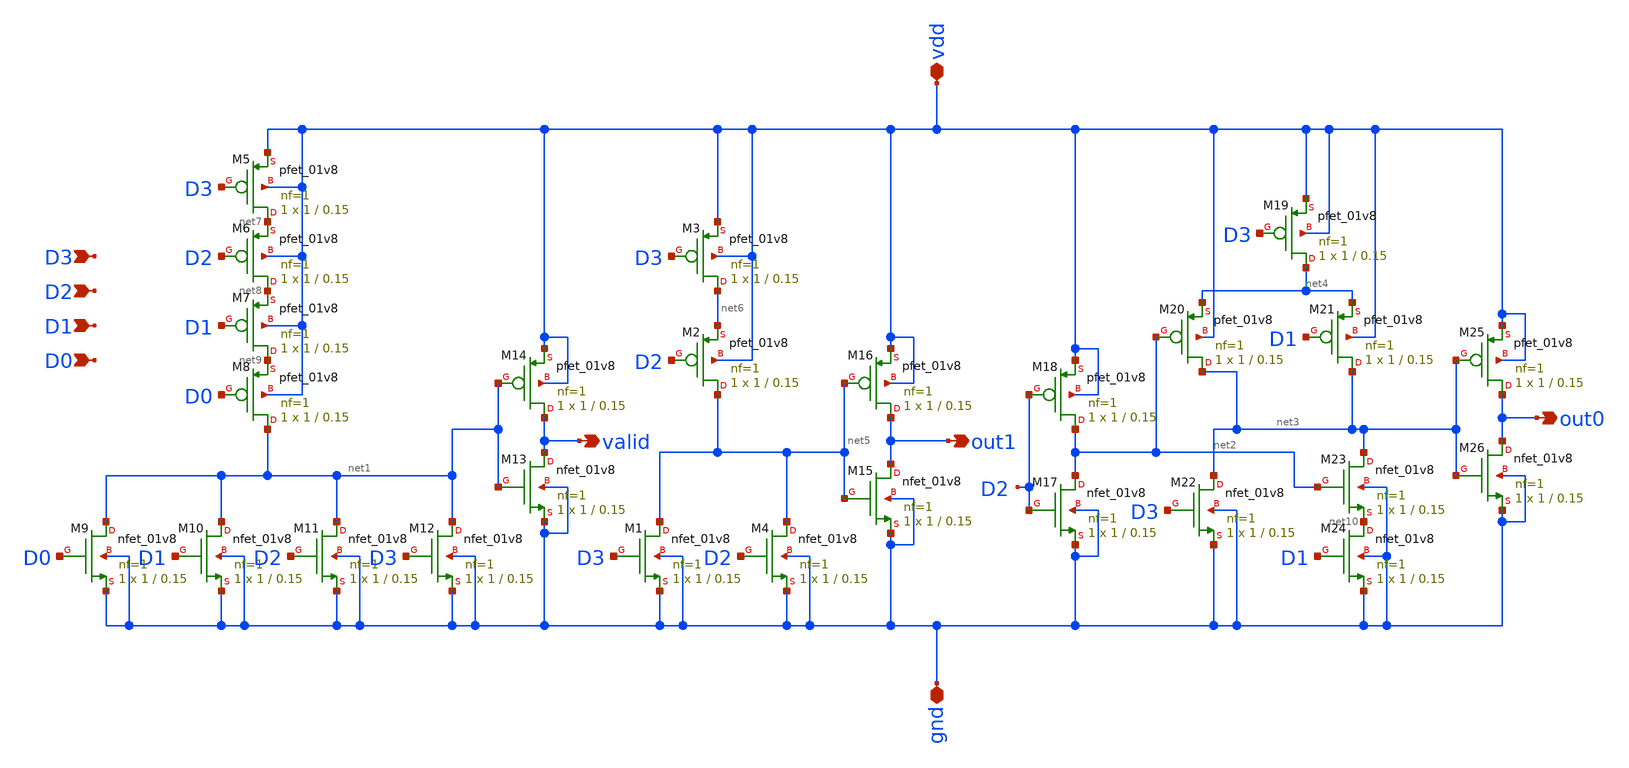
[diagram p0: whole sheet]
** sch_path: Primitives/Priority Encoder 4to2/Xschem Files/P_enc_4to2.sch
**.subckt P_enc_4to2 valid vdd gnd out1 out0 D3 D2 D1 D0
*.opin valid
*.iopin vdd
*.iopin gnd
*.opin out1
*.opin out0
*.ipin D3
*.ipin D2
*.ipin D1
*.ipin D0
XM5 net7 D3 vdd vdd sky130_fd_pr__pfet_01v8 L=0.15 W=1 nf=1 ad='int((1 + 1)/2) * 1 / 1 * 0.29' as='int((1 + 2)/2) * 1 / 1 * 0.29'
+ pd='2*int((1 + 1)/2) * (1 / 1 + 0.29)' ps='2*int((1 + 2)/2) * (1 / 1 + 0.29)' nrd='0.29 / 1 ' nrs='0.29 / 1 '
+ sa=0 sb=0 sd=0 mult=1 m=1
XM6 net8 D2 net7 vdd sky130_fd_pr__pfet_01v8 L=0.15 W=1 nf=1 ad='int((1 + 1)/2) * 1 / 1 * 0.29' as='int((1 + 2)/2) * 1 / 1 * 0.29'
+ pd='2*int((1 + 1)/2) * (1 / 1 + 0.29)' ps='2*int((1 + 2)/2) * (1 / 1 + 0.29)' nrd='0.29 / 1 ' nrs='0.29 / 1 '
+ sa=0 sb=0 sd=0 mult=1 m=1
XM7 net9 D1 net8 vdd sky130_fd_pr__pfet_01v8 L=0.15 W=1 nf=1 ad='int((1 + 1)/2) * 1 / 1 * 0.29' as='int((1 + 2)/2) * 1 / 1 * 0.29'
+ pd='2*int((1 + 1)/2) * (1 / 1 + 0.29)' ps='2*int((1 + 2)/2) * (1 / 1 + 0.29)' nrd='0.29 / 1 ' nrs='0.29 / 1 '
+ sa=0 sb=0 sd=0 mult=1 m=1
XM8 net1 D0 net9 vdd sky130_fd_pr__pfet_01v8 L=0.15 W=1 nf=1 ad='int((1 + 1)/2) * 1 / 1 * 0.29' as='int((1 + 2)/2) * 1 / 1 * 0.29'
+ pd='2*int((1 + 1)/2) * (1 / 1 + 0.29)' ps='2*int((1 + 2)/2) * (1 / 1 + 0.29)' nrd='0.29 / 1 ' nrs='0.29 / 1 '
+ sa=0 sb=0 sd=0 mult=1 m=1
XM9 net1 D0 gnd gnd sky130_fd_pr__nfet_01v8 L=0.15 W=1 nf=1 ad='int((1 + 1)/2) * 1 / 1 * 0.29' as='int((1 + 2)/2) * 1 / 1 * 0.29'
+ pd='2*int((1 + 1)/2) * (1 / 1 + 0.29)' ps='2*int((1 + 2)/2) * (1 / 1 + 0.29)' nrd='0.29 / 1 ' nrs='0.29 / 1 '
+ sa=0 sb=0 sd=0 mult=1 m=1
XM10 net1 D1 gnd gnd sky130_fd_pr__nfet_01v8 L=0.15 W=1 nf=1 ad='int((1 + 1)/2) * 1 / 1 * 0.29' as='int((1 + 2)/2) * 1 / 1 * 0.29'
+ pd='2*int((1 + 1)/2) * (1 / 1 + 0.29)' ps='2*int((1 + 2)/2) * (1 / 1 + 0.29)' nrd='0.29 / 1 ' nrs='0.29 / 1 '
+ sa=0 sb=0 sd=0 mult=1 m=1
XM11 net1 D2 gnd gnd sky130_fd_pr__nfet_01v8 L=0.15 W=1 nf=1 ad='int((1 + 1)/2) * 1 / 1 * 0.29' as='int((1 + 2)/2) * 1 / 1 * 0.29'
+ pd='2*int((1 + 1)/2) * (1 / 1 + 0.29)' ps='2*int((1 + 2)/2) * (1 / 1 + 0.29)' nrd='0.29 / 1 ' nrs='0.29 / 1 '
+ sa=0 sb=0 sd=0 mult=1 m=1
XM12 net1 D3 gnd gnd sky130_fd_pr__nfet_01v8 L=0.15 W=1 nf=1 ad='int((1 + 1)/2) * 1 / 1 * 0.29' as='int((1 + 2)/2) * 1 / 1 * 0.29'
+ pd='2*int((1 + 1)/2) * (1 / 1 + 0.29)' ps='2*int((1 + 2)/2) * (1 / 1 + 0.29)' nrd='0.29 / 1 ' nrs='0.29 / 1 '
+ sa=0 sb=0 sd=0 mult=1 m=1
XM13 valid net1 gnd gnd sky130_fd_pr__nfet_01v8 L=0.15 W=1 nf=1 ad='int((1 + 1)/2) * 1 / 1 * 0.29' as='int((1 + 2)/2) * 1 / 1 * 0.29'
+ pd='2*int((1 + 1)/2) * (1 / 1 + 0.29)' ps='2*int((1 + 2)/2) * (1 / 1 + 0.29)' nrd='0.29 / 1 ' nrs='0.29 / 1 '
+ sa=0 sb=0 sd=0 mult=1 m=1
XM14 valid net1 vdd vdd sky130_fd_pr__pfet_01v8 L=0.15 W=1 nf=1 ad='int((1 + 1)/2) * 1 / 1 * 0.29' as='int((1 + 2)/2) * 1 / 1 * 0.29'
+ pd='2*int((1 + 1)/2) * (1 / 1 + 0.29)' ps='2*int((1 + 2)/2) * (1 / 1 + 0.29)' nrd='0.29 / 1 ' nrs='0.29 / 1 '
+ sa=0 sb=0 sd=0 mult=1 m=1
XM17 net2 D2 gnd gnd sky130_fd_pr__nfet_01v8 L=0.15 W=1 nf=1 ad='int((1 + 1)/2) * 1 / 1 * 0.29' as='int((1 + 2)/2) * 1 / 1 * 0.29'
+ pd='2*int((1 + 1)/2) * (1 / 1 + 0.29)' ps='2*int((1 + 2)/2) * (1 / 1 + 0.29)' nrd='0.29 / 1 ' nrs='0.29 / 1 '
+ sa=0 sb=0 sd=0 mult=1 m=1
XM18 net2 D2 vdd vdd sky130_fd_pr__pfet_01v8 L=0.15 W=1 nf=1 ad='int((1 + 1)/2) * 1 / 1 * 0.29' as='int((1 + 2)/2) * 1 / 1 * 0.29'
+ pd='2*int((1 + 1)/2) * (1 / 1 + 0.29)' ps='2*int((1 + 2)/2) * (1 / 1 + 0.29)' nrd='0.29 / 1 ' nrs='0.29 / 1 '
+ sa=0 sb=0 sd=0 mult=1 m=1
XM19 net4 D3 vdd vdd sky130_fd_pr__pfet_01v8 L=0.15 W=1 nf=1 ad='int((1 + 1)/2) * 1 / 1 * 0.29' as='int((1 + 2)/2) * 1 / 1 * 0.29'
+ pd='2*int((1 + 1)/2) * (1 / 1 + 0.29)' ps='2*int((1 + 2)/2) * (1 / 1 + 0.29)' nrd='0.29 / 1 ' nrs='0.29 / 1 '
+ sa=0 sb=0 sd=0 mult=1 m=1
XM20 net3 net2 net4 vdd sky130_fd_pr__pfet_01v8 L=0.15 W=1 nf=1 ad='int((1 + 1)/2) * 1 / 1 * 0.29' as='int((1 + 2)/2) * 1 / 1 * 0.29'
+ pd='2*int((1 + 1)/2) * (1 / 1 + 0.29)' ps='2*int((1 + 2)/2) * (1 / 1 + 0.29)' nrd='0.29 / 1 ' nrs='0.29 / 1 '
+ sa=0 sb=0 sd=0 mult=1 m=1
XM21 net3 D1 net4 vdd sky130_fd_pr__pfet_01v8 L=0.15 W=1 nf=1 ad='int((1 + 1)/2) * 1 / 1 * 0.29' as='int((1 + 2)/2) * 1 / 1 * 0.29'
+ pd='2*int((1 + 1)/2) * (1 / 1 + 0.29)' ps='2*int((1 + 2)/2) * (1 / 1 + 0.29)' nrd='0.29 / 1 ' nrs='0.29 / 1 '
+ sa=0 sb=0 sd=0 mult=1 m=1
XM22 net3 D3 gnd gnd sky130_fd_pr__nfet_01v8 L=0.15 W=1 nf=1 ad='int((1 + 1)/2) * 1 / 1 * 0.29' as='int((1 + 2)/2) * 1 / 1 * 0.29'
+ pd='2*int((1 + 1)/2) * (1 / 1 + 0.29)' ps='2*int((1 + 2)/2) * (1 / 1 + 0.29)' nrd='0.29 / 1 ' nrs='0.29 / 1 '
+ sa=0 sb=0 sd=0 mult=1 m=1
XM23 net3 net2 net10 gnd sky130_fd_pr__nfet_01v8 L=0.15 W=1 nf=1 ad='int((1 + 1)/2) * 1 / 1 * 0.29' as='int((1 + 2)/2) * 1 / 1 * 0.29'
+ pd='2*int((1 + 1)/2) * (1 / 1 + 0.29)' ps='2*int((1 + 2)/2) * (1 / 1 + 0.29)' nrd='0.29 / 1 ' nrs='0.29 / 1 '
+ sa=0 sb=0 sd=0 mult=1 m=1
XM24 net10 D1 gnd gnd sky130_fd_pr__nfet_01v8 L=0.15 W=1 nf=1 ad='int((1 + 1)/2) * 1 / 1 * 0.29' as='int((1 + 2)/2) * 1 / 1 * 0.29'
+ pd='2*int((1 + 1)/2) * (1 / 1 + 0.29)' ps='2*int((1 + 2)/2) * (1 / 1 + 0.29)' nrd='0.29 / 1 ' nrs='0.29 / 1 '
+ sa=0 sb=0 sd=0 mult=1 m=1
XM25 out0 net3 vdd vdd sky130_fd_pr__pfet_01v8 L=0.15 W=1 nf=1 ad='int((1 + 1)/2) * 1 / 1 * 0.29' as='int((1 + 2)/2) * 1 / 1 * 0.29'
+ pd='2*int((1 + 1)/2) * (1 / 1 + 0.29)' ps='2*int((1 + 2)/2) * (1 / 1 + 0.29)' nrd='0.29 / 1 ' nrs='0.29 / 1 '
+ sa=0 sb=0 sd=0 mult=1 m=1
XM26 out0 net3 gnd gnd sky130_fd_pr__nfet_01v8 L=0.15 W=1 nf=1 ad='int((1 + 1)/2) * 1 / 1 * 0.29' as='int((1 + 2)/2) * 1 / 1 * 0.29'
+ pd='2*int((1 + 1)/2) * (1 / 1 + 0.29)' ps='2*int((1 + 2)/2) * (1 / 1 + 0.29)' nrd='0.29 / 1 ' nrs='0.29 / 1 '
+ sa=0 sb=0 sd=0 mult=1 m=1
XM1 net5 D3 gnd gnd sky130_fd_pr__nfet_01v8 L=0.15 W=1 nf=1 ad='int((1 + 1)/2) * 1 / 1 * 0.29' as='int((1 + 2)/2) * 1 / 1 * 0.29'
+ pd='2*int((1 + 1)/2) * (1 / 1 + 0.29)' ps='2*int((1 + 2)/2) * (1 / 1 + 0.29)' nrd='0.29 / 1 ' nrs='0.29 / 1 '
+ sa=0 sb=0 sd=0 mult=1 m=1
XM2 net5 D2 net6 vdd sky130_fd_pr__pfet_01v8 L=0.15 W=1 nf=1 ad='int((1 + 1)/2) * 1 / 1 * 0.29' as='int((1 + 2)/2) * 1 / 1 * 0.29'
+ pd='2*int((1 + 1)/2) * (1 / 1 + 0.29)' ps='2*int((1 + 2)/2) * (1 / 1 + 0.29)' nrd='0.29 / 1 ' nrs='0.29 / 1 '
+ sa=0 sb=0 sd=0 mult=1 m=1
XM3 net6 D3 vdd vdd sky130_fd_pr__pfet_01v8 L=0.15 W=1 nf=1 ad='int((1 + 1)/2) * 1 / 1 * 0.29' as='int((1 + 2)/2) * 1 / 1 * 0.29'
+ pd='2*int((1 + 1)/2) * (1 / 1 + 0.29)' ps='2*int((1 + 2)/2) * (1 / 1 + 0.29)' nrd='0.29 / 1 ' nrs='0.29 / 1 '
+ sa=0 sb=0 sd=0 mult=1 m=1
XM4 net5 D2 gnd gnd sky130_fd_pr__nfet_01v8 L=0.15 W=1 nf=1 ad='int((1 + 1)/2) * 1 / 1 * 0.29' as='int((1 + 2)/2) * 1 / 1 * 0.29'
+ pd='2*int((1 + 1)/2) * (1 / 1 + 0.29)' ps='2*int((1 + 2)/2) * (1 / 1 + 0.29)' nrd='0.29 / 1 ' nrs='0.29 / 1 '
+ sa=0 sb=0 sd=0 mult=1 m=1
XM15 out1 net5 gnd gnd sky130_fd_pr__nfet_01v8 L=0.15 W=1 nf=1 ad='int((1 + 1)/2) * 1 / 1 * 0.29' as='int((1 + 2)/2) * 1 / 1 * 0.29'
+ pd='2*int((1 + 1)/2) * (1 / 1 + 0.29)' ps='2*int((1 + 2)/2) * (1 / 1 + 0.29)' nrd='0.29 / 1 ' nrs='0.29 / 1 '
+ sa=0 sb=0 sd=0 mult=1 m=1
XM16 out1 net5 vdd vdd sky130_fd_pr__pfet_01v8 L=0.15 W=1 nf=1 ad='int((1 + 1)/2) * 1 / 1 * 0.29' as='int((1 + 2)/2) * 1 / 1 * 0.29'
+ pd='2*int((1 + 1)/2) * (1 / 1 + 0.29)' ps='2*int((1 + 2)/2) * (1 / 1 + 0.29)' nrd='0.29 / 1 ' nrs='0.29 / 1 '
+ sa=0 sb=0 sd=0 mult=1 m=1
**.ends
.end
